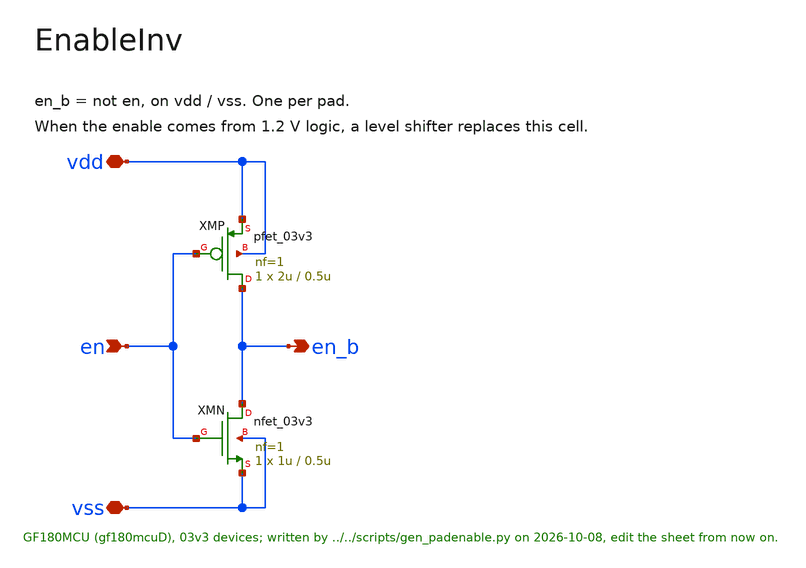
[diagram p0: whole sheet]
** sch_path: macros/PadEnable/schematic/xschem/EnableInv.sch
**.subckt EnableInv vdd vss en en_b
*.iopin vdd
*.iopin vss
*.ipin en
*.opin en_b
XMP en_b en vdd vdd pfet_03v3 L=0.5u W=2u nf=1 ad='int((nf+1)/2) * W/nf * 0.18u' as='int((nf+2)/2) * W/nf * 0.18u'
+ pd='2*int((nf+1)/2) * (W/nf + 0.18u)' ps='2*int((nf+2)/2) * (W/nf + 0.18u)' nrd='0.18u / W' nrs='0.18u / W'
+ sa=0 sb=0 sd=0 m=1
XMN en_b en vss vss nfet_03v3 L=0.5u W=1u nf=1 ad='int((nf+1)/2) * W/nf * 0.18u' as='int((nf+2)/2) * W/nf * 0.18u'
+ pd='2*int((nf+1)/2) * (W/nf + 0.18u)' ps='2*int((nf+2)/2) * (W/nf + 0.18u)' nrd='0.18u / W' nrs='0.18u / W'
+ sa=0 sb=0 sd=0 m=1
**.ends
.end
